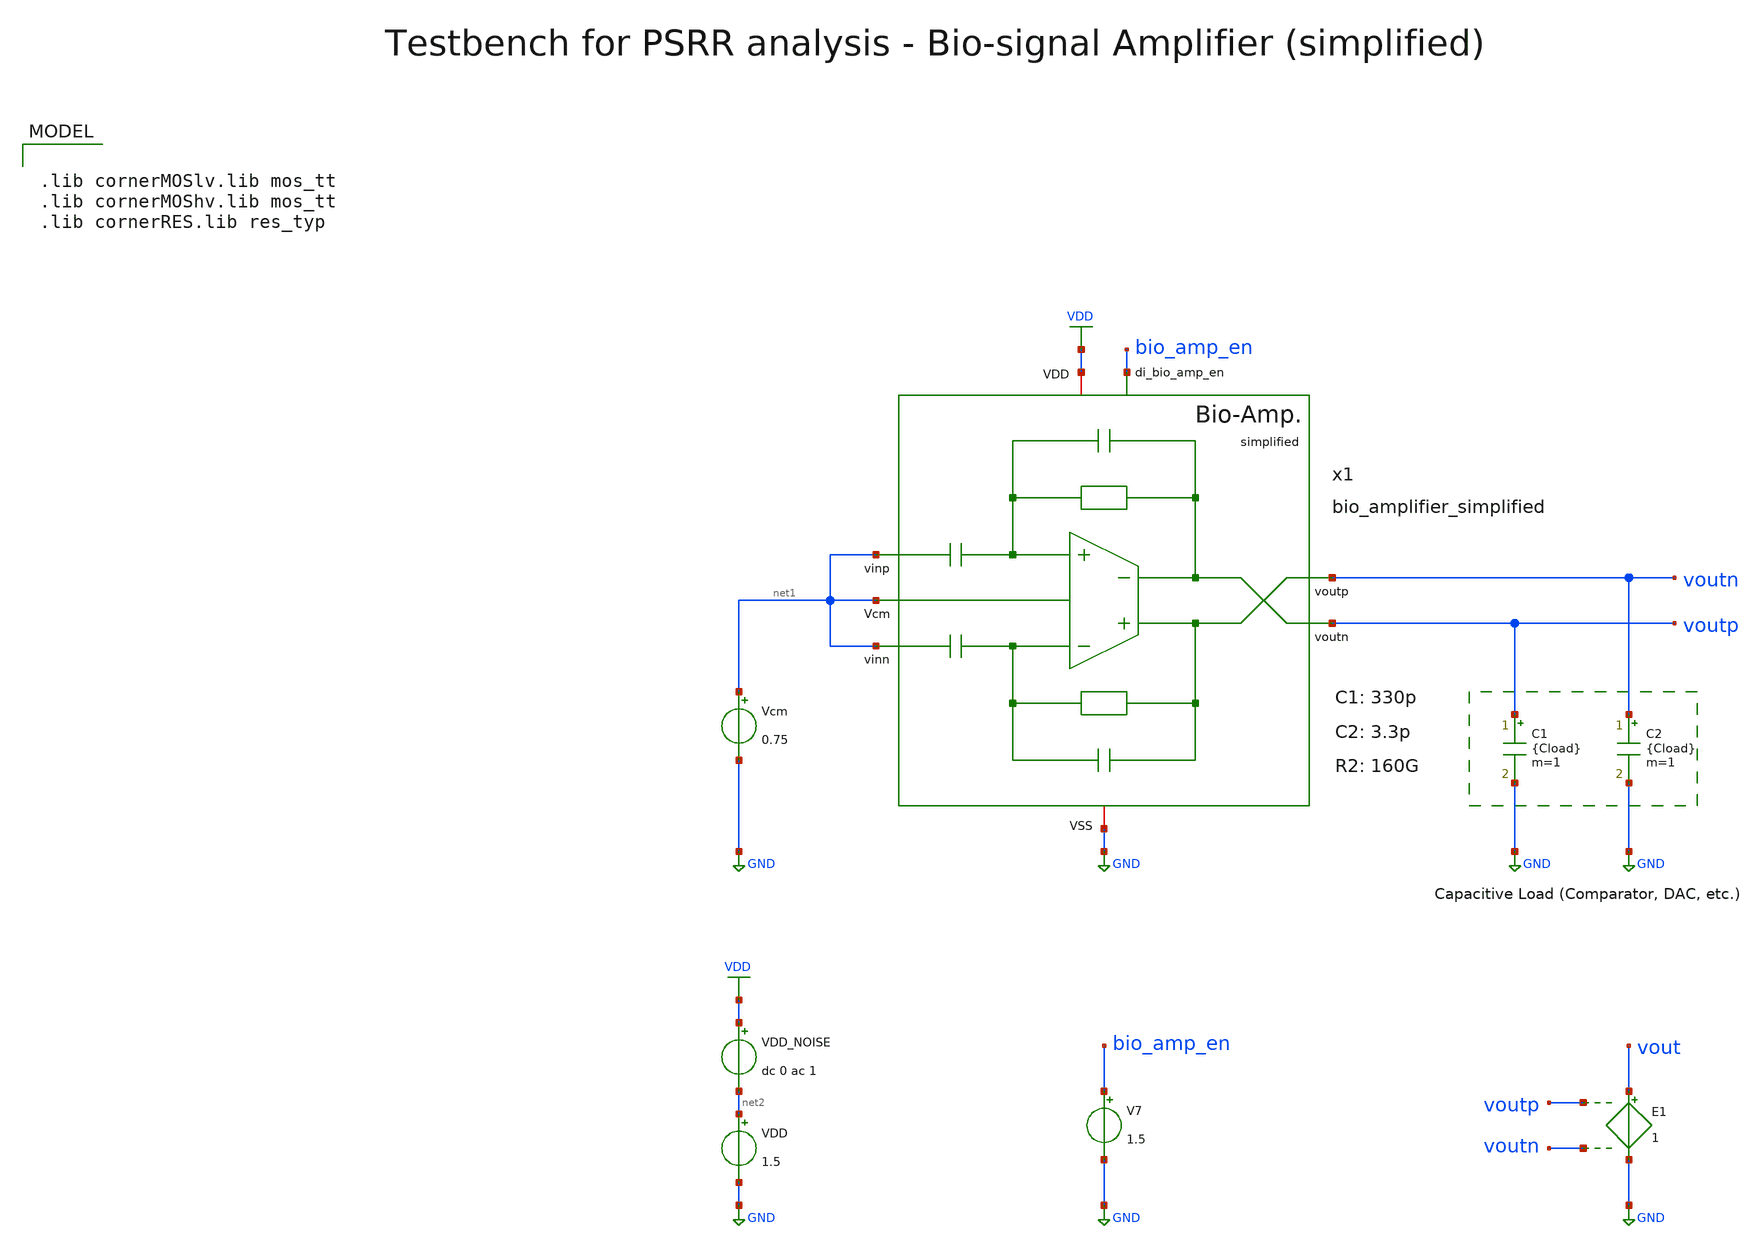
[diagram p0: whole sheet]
** sch_path: SG13G2_ATBS-ADC-main/xschem/bio_amplifier/testbenches/bio_amplifier_simplified_tb_PSRR.sch
**.subckt bio_amplifier_simplified_tb_PSRR
C1 voutp GND {Cload} m=1
C2 voutn GND {Cload} m=1
Vcm net1 GND 0.75
E1 vout GND voutp voutn 1
VDD net2 GND 1.5
VDD_NOISE VDD net2 dc 0 ac 1
V7 bio_amp_en GND 1.5
x1 voutn bio_amp_en net1 net1 voutp net1 VDD GND bio_amplifier_simplified C1=330p C2=3.3p R2=160G
**** begin user architecture code


.param temp=27
* 227.56fF DAC
.param Cload=227.56f
.options savecurrents method=gear reltol=1e-2 abstol=1e-15 gmin=1e-15 rshunt=1e15
.control

optran 0 0 0 1u 1m 0

save v(VDD) v(vout) v(voutp) v(voutn)

* User Constants
let f_min = 10m
let f_max = 1G
let fdc = 1

* Operating Point Analysis
op
remzerovec
write bio_amplifier_simplified_tb_PSRR.raw
set appendwrite

* AC Analysis
ac dec 101 $&const.f_min $&const.f_max
remzerovec
write bio_amplifier_simplified_tb_PSRR.raw

* Plotting
let PSRR = v(VDD)/v(vout)
let PSRRp = v(VDD)/v(voutp)
let PSRRn = v(VDD)/v(voutn)

let PSRR_dB = vdb(PSRR)
let PSRRp_dB = vdb(PSRRp)
let PSRRn_dB = vdb(PSRRn)

plot PSRR_dB PSRRp_dB PSRRn_dB ylabel 'PSRR, PSRR+, PSRR-'

* Measurements
meas ac PSRRdc_dB find PSRR_dB when frequency = fdc
print PSRRdc_dB

meas ac PSRRpdc_dB find PSRRp_dB when frequency = fdc
print PSRRpdc_dB

meas ac PSRRndc_dB find PSRRn_dB when frequency = fdc
print PSRRndc_dB

* Write Data
set wr_vecnames
set wr_singlescale
wrdata
+ /foss/designs/SG13G2_ATBS-ADC-main/python/plot_simulations/data/bio_amplifier_simplified_tb_PSRR.txt v(PSRR_dB)

*quit
.endc



.lib cornerMOSlv.lib mos_tt
.lib cornerMOShv.lib mos_tt
.lib cornerRES.lib res_typ

**** end user architecture code
**.ends
.GLOBAL GND
.GLOBAL VDD
.end
